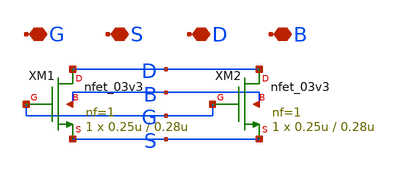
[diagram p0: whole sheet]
** sch_path: DAC_PAKISTAN_01/Pakistan1_Xschem/nfet_03V3_f2.sch
**.subckt nfet_03V3_f2 G S D B
*.iopin G
*.iopin S
*.iopin D
*.iopin B
XM1 D G S B nfet_03v3 L=0.28u W=0.25u nf=1 ad='int((nf+1)/2) * W/nf * 0.18u' as='int((nf+2)/2) * W/nf * 0.18u'
+ pd='2*int((nf+1)/2) * (W/nf + 0.18u)' ps='2*int((nf+2)/2) * (W/nf + 0.18u)' nrd='0.18u / W' nrs='0.18u / W'
+ sa=0 sb=0 sd=0 m=1
XM2 D G S B nfet_03v3 L=0.28u W=0.25u nf=1 ad='int((nf+1)/2) * W/nf * 0.18u' as='int((nf+2)/2) * W/nf * 0.18u'
+ pd='2*int((nf+1)/2) * (W/nf + 0.18u)' ps='2*int((nf+2)/2) * (W/nf + 0.18u)' nrd='0.18u / W' nrs='0.18u / W'
+ sa=0 sb=0 sd=0 m=1
**.ends
.end
